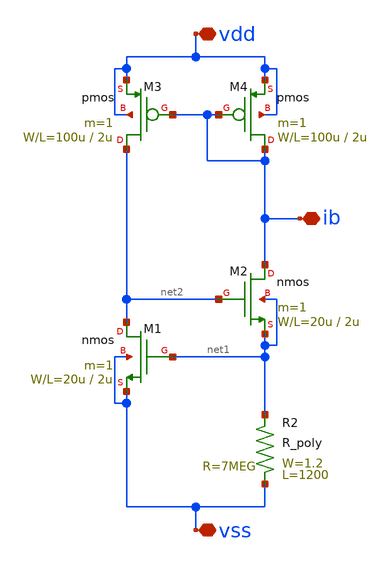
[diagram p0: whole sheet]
** sch_path: OR1/PTC06/opamp/cs-vth-ref_sym.sch
**.subckt cs-vth-ref_sym vdd vss ib
*.iopin vdd
*.iopin vss
*.iopin ib
R2 vss net1 R_poly W=1.2 L=1200
M4 ib ib vdd vdd pmos L=2u W=100u m=1
M3 net2 ib vdd vdd pmos L=2u W=100u m=1
M2 ib net2 net1 net1 nmos L=2u W=20u m=1
M1 net2 net1 vss vss nmos L=2u W=20u m=1
**.ends
.end
